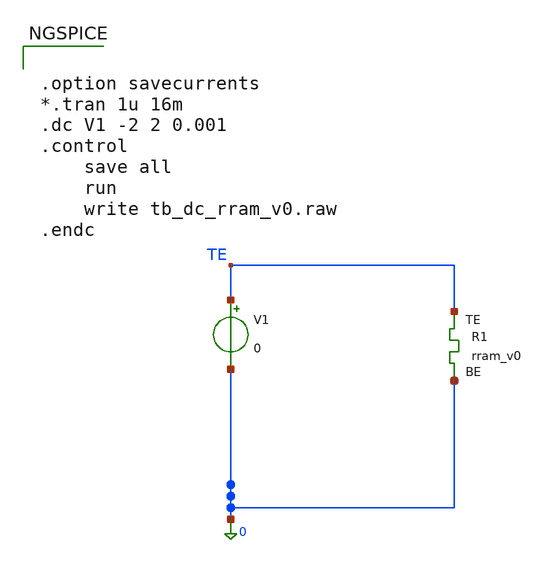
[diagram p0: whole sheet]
** sch_path: memristor_models/wellposed/tb_dc_rram_v0.sch
**.subckt tb_dc_rram_v0
V1 TE 0 0
XR1 TE 0 rram_v0
**** begin user architecture code

** opencircuitdesign pdks install
.inc $::SKYWATER_MODELS/rram_v0.spice



.option savecurrents
*.tran 1u 16m
.dc V1 -2 2 0.001
.control
	save all
	run
	write tb_dc_rram_v0.raw
.endc



**** end user architecture code
**.ends
.end
